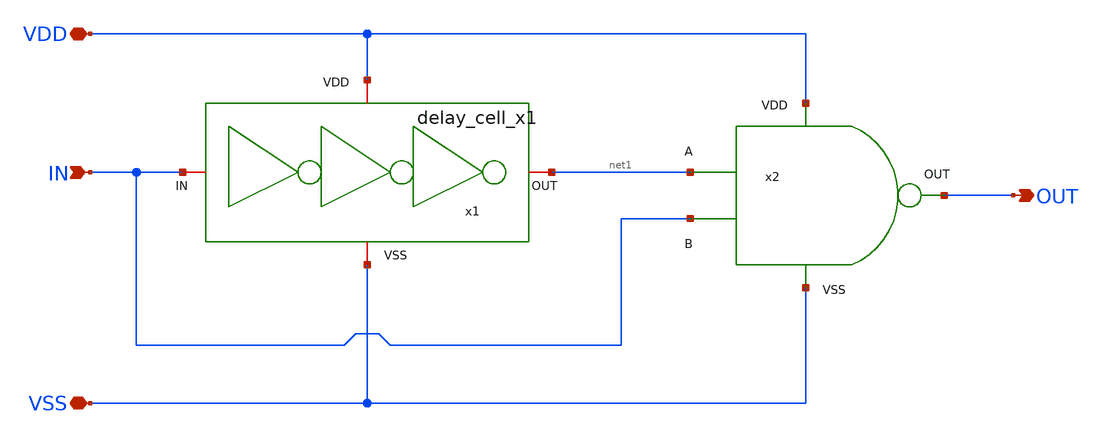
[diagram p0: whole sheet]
** sch_path: designs/sar_adc/digital/edge_detector/xschem/edge_detector.sch
**.subckt edge_detector VDD VSS IN OUT
*.iopin VDD
*.iopin VSS
*.ipin IN
*.opin OUT
x1 VDD IN net1 VSS delay_cell_x1
x2 VDD VSS net1 IN OUT NAND
**.ends

* expanding   symbol:  designs/sar_adc/digital/delay_cell/xschem/delay_cell_x1.sym # of pins=4
** sym_path: designs/sar_adc/digital/delay_cell/xschem/delay_cell_x1.sym
** sch_path: designs/sar_adc/digital/delay_cell/xschem/delay_cell_x1.sch
.subckt delay_cell_x1 VDD IN OUT VSS
*.iopin IN
*.iopin OUT
*.iopin VDD
*.iopin VSS
x1 VDD IN net2 VSS inverter
x2 VDD net2 net3 VSS inverter
x3 VDD net3 net4 VSS inverter
x4 VDD net4 net1 VSS inverter
x5 VDD net1 OUT VSS inverter
.ends


* expanding   symbol:  designs/sar_adc/digital/nand_edge/xschem/NAND.sym # of pins=5
** sym_path: designs/sar_adc/digital/NAND/xschem/NAND.sym
** sch_path: designs/sar_adc/digital/NAND/xschem/NAND.sch
.subckt NAND VDD VSS A B out
*.iopin VDD
*.iopin A
*.iopin B
*.iopin out
*.iopin VSS
xINVA VDD net1 net2 VSS inverter
xINVB[2] VDD net2 out VSS inverter
xINVB[1] VDD net2 out VSS inverter
xINVB[0] VDD net2 out VSS inverter
XM2 net1 A VDD VDD pfet_03v3 L=0.28u W=0.5u nf=1 ad='int((nf+1)/2) * W/nf * 0.18u' as='int((nf+2)/2) * W/nf * 0.18u'
+ pd='2*int((nf+1)/2) * (W/nf + 0.18u)' ps='2*int((nf+2)/2) * (W/nf + 0.18u)' nrd='0.18u / W' nrs='0.18u / W'
+ sa=0 sb=0 sd=0 m=2
XM1 net1 A net3 VSS nfet_03v3 L=0.28u W=0.5u nf=1 ad='int((nf+1)/2) * W/nf * 0.18u' as='int((nf+2)/2) * W/nf * 0.18u'
+ pd='2*int((nf+1)/2) * (W/nf + 0.18u)' ps='2*int((nf+2)/2) * (W/nf + 0.18u)' nrd='0.18u / W' nrs='0.18u / W'
+ sa=0 sb=0 sd=0 m=1
XM3 net1 B VDD VDD pfet_03v3 L=0.28u W=0.5u nf=1 ad='int((nf+1)/2) * W/nf * 0.18u' as='int((nf+2)/2) * W/nf * 0.18u'
+ pd='2*int((nf+1)/2) * (W/nf + 0.18u)' ps='2*int((nf+2)/2) * (W/nf + 0.18u)' nrd='0.18u / W' nrs='0.18u / W'
+ sa=0 sb=0 sd=0 m=2
XM4 net3 B VSS VSS nfet_03v3 L=0.28u W=0.5u nf=1 ad='int((nf+1)/2) * W/nf * 0.18u' as='int((nf+2)/2) * W/nf * 0.18u'
+ pd='2*int((nf+1)/2) * (W/nf + 0.18u)' ps='2*int((nf+2)/2) * (W/nf + 0.18u)' nrd='0.18u / W' nrs='0.18u / W'
+ sa=0 sb=0 sd=0 m=1
.ends


* expanding   symbol:  designs/sar_adc/digital/edge_inv_x1/xschem/inverter.sym # of pins=6
** sym_path: designs/sar_adc/digital/inverter/xschem/inverter.sym
** sch_path: designs/sar_adc/digital/inverter/xschem/inverter.sch
.subckt inverter VDD in out VSS
*.opin out
*.iopin in
*.iopin VDD
*.iopin VSS
XM1 out in VSS VSS nfet_03v3 L=0.28u W=1u nf=1 ad='int((nf+1)/2) * W/nf * 0.18u' as='int((nf+2)/2) * W/nf * 0.18u'
+ pd='2*int((nf+1)/2) * (W/nf + 0.18u)' ps='2*int((nf+2)/2) * (W/nf + 0.18u)' nrd='0.18u / W' nrs='0.18u / W'
+ sa=0 sb=0 sd=0 m=1
XM2 out in VDD VDD pfet_03v3 L=0.28u W=3u nf=1 ad='int((nf+1)/2) * W/nf * 0.18u' as='int((nf+2)/2) * W/nf * 0.18u'
+ pd='2*int((nf+1)/2) * (W/nf + 0.18u)' ps='2*int((nf+2)/2) * (W/nf + 0.18u)' nrd='0.18u / W' nrs='0.18u / W'
+ sa=0 sb=0 sd=0 m=1
.ends

.end
